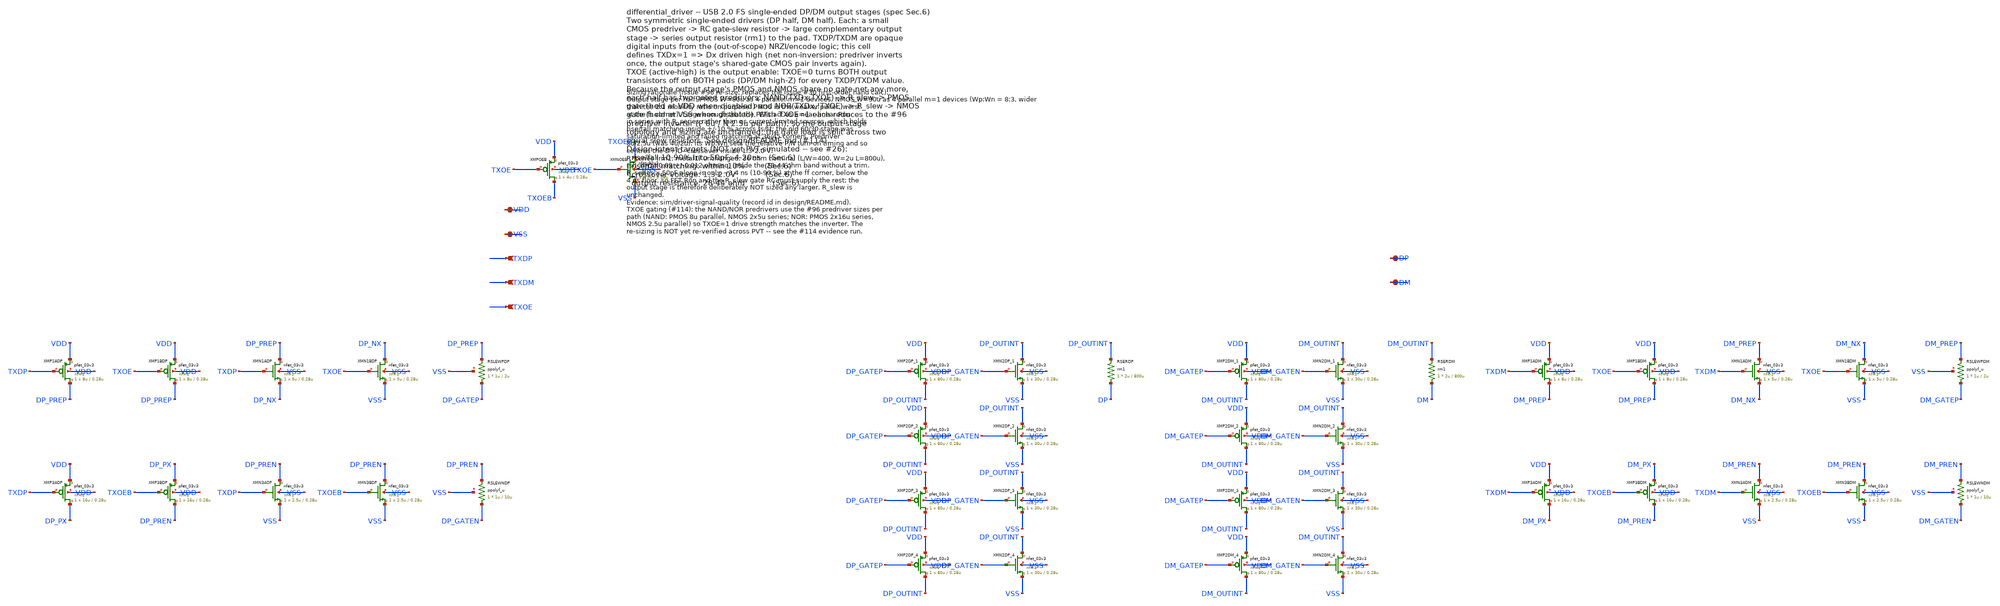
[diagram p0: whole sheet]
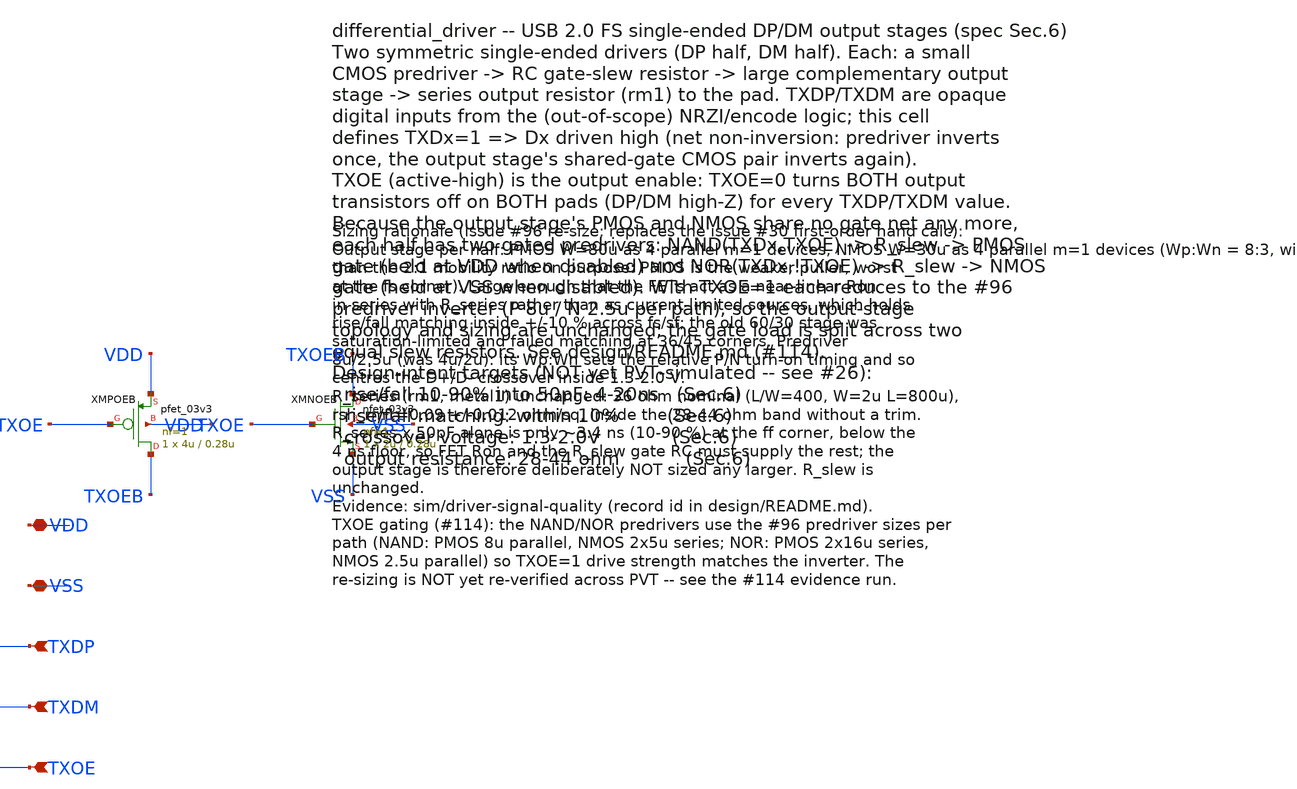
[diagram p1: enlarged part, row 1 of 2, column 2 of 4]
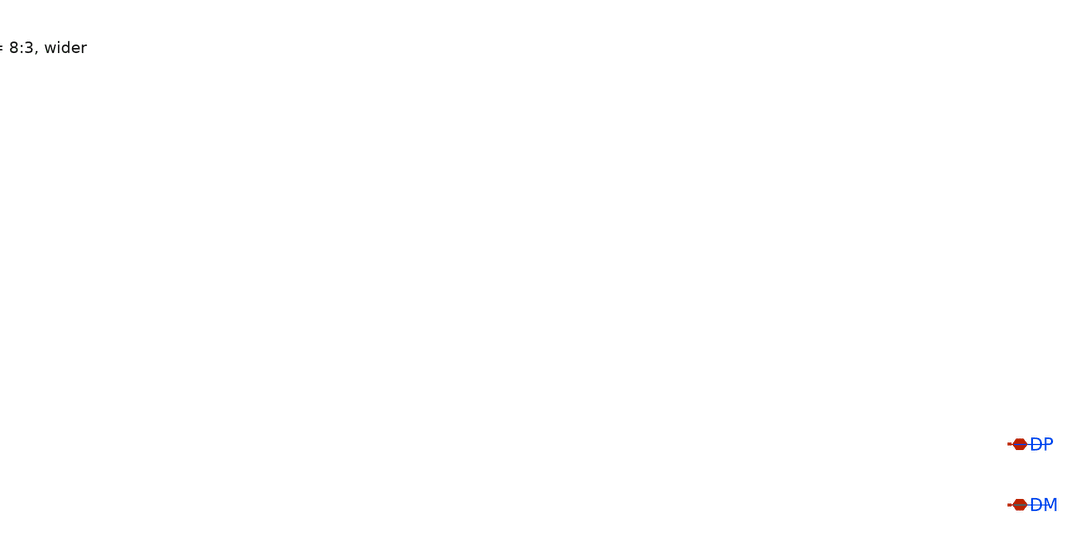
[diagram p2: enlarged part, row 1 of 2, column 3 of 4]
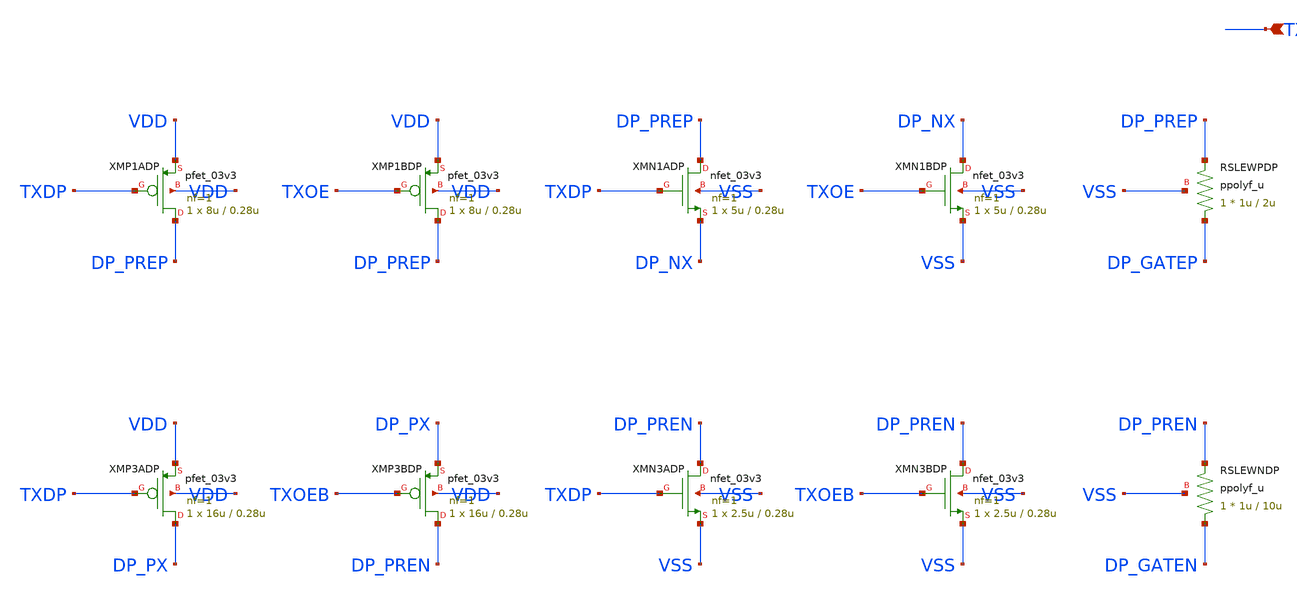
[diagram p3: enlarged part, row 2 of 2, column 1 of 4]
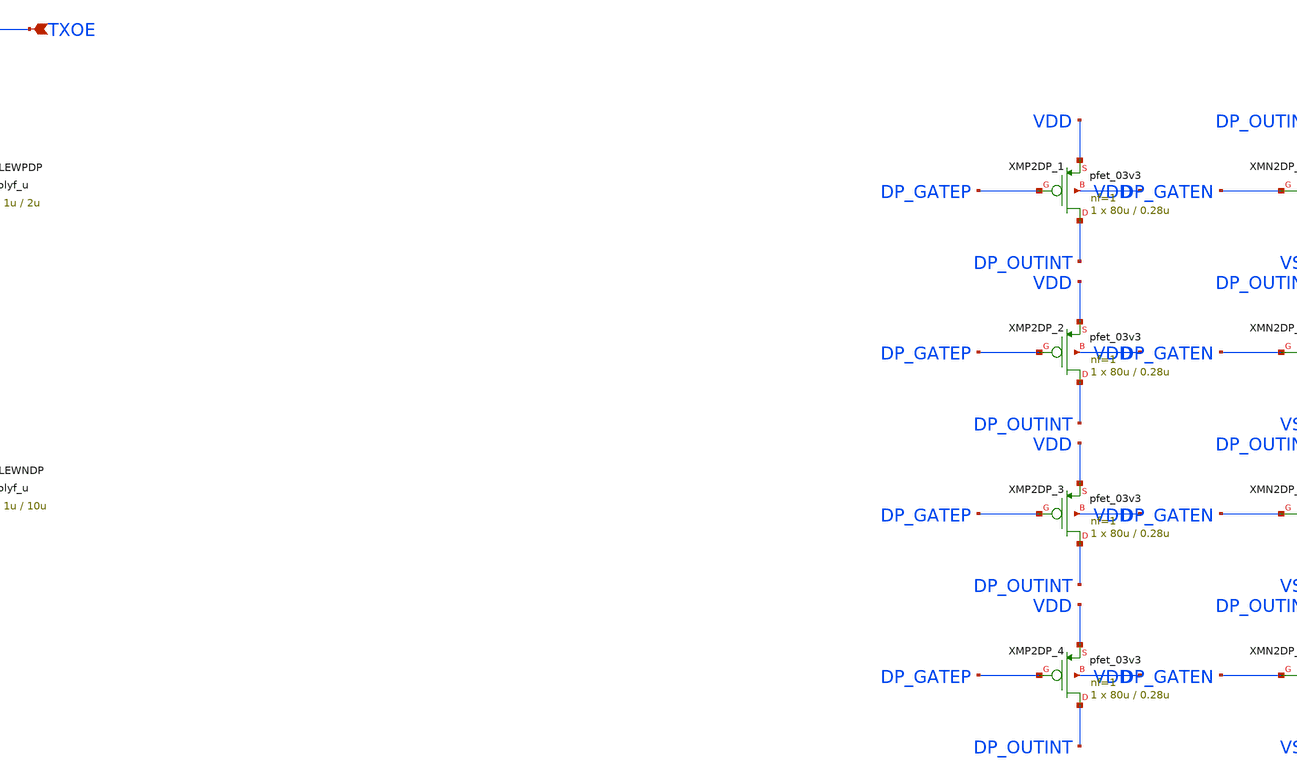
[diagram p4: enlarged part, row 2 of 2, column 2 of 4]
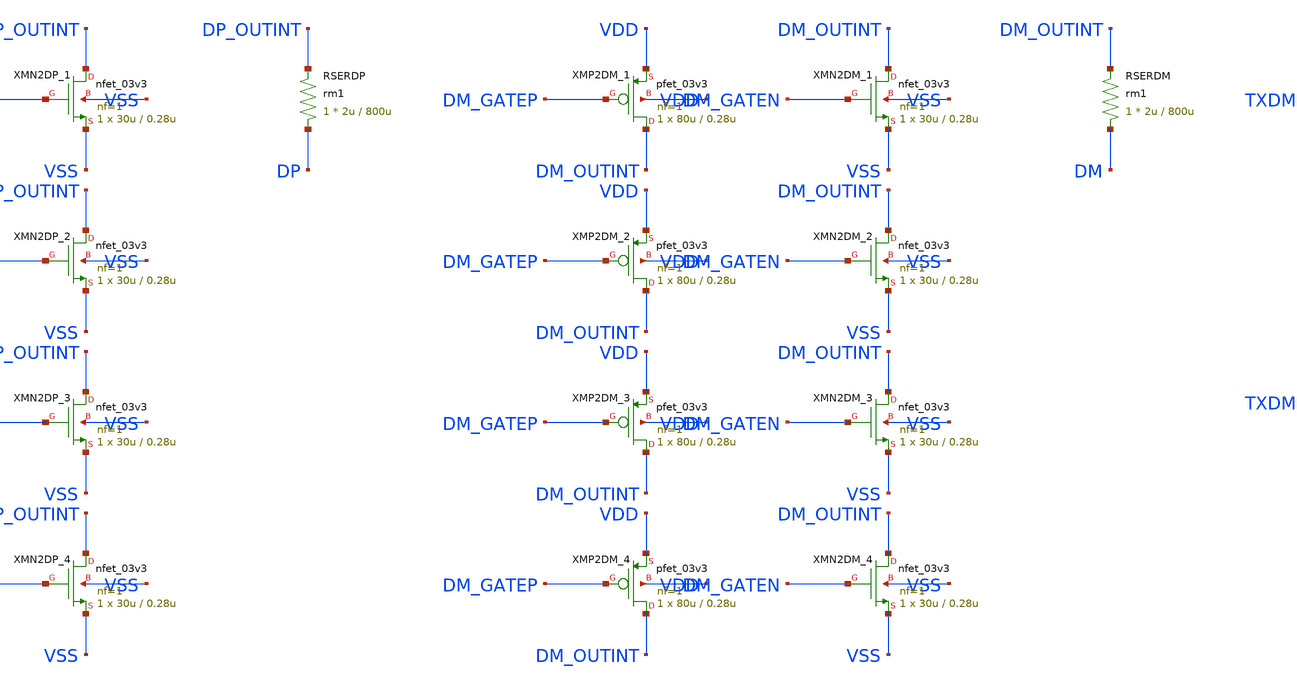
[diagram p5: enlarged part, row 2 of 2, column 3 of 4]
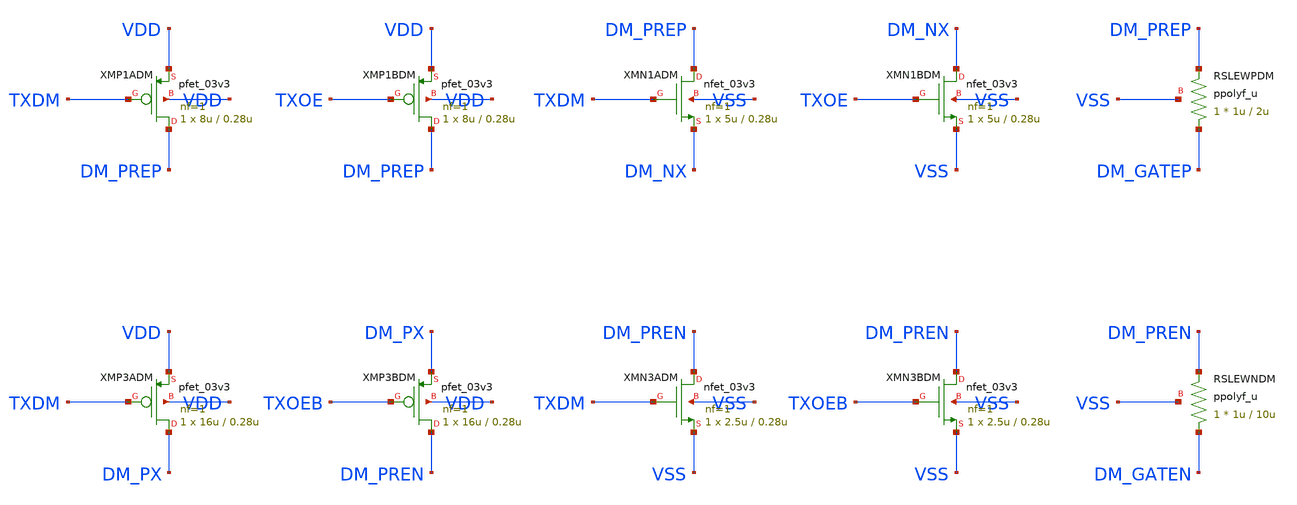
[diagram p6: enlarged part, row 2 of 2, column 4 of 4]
** sch_path: design/differential_driver.sch
**.subckt differential_driver VDD VSS TXDP TXDM TXOE DP DM
*.iopin VDD
*.iopin VSS
*.ipin TXDP
*.ipin TXDM
*.ipin TXOE
*.iopin DP
*.iopin DM
XMPOEB TXOEB TXOE VDD VDD pfet_03v3 L=0.28u W=4u nf=1 ad='int((nf+1)/2) * W/nf * 0.18u' as='int((nf+2)/2) * W/nf * 0.18u'
+ pd='2*int((nf+1)/2) * (W/nf + 0.18u)' ps='2*int((nf+2)/2) * (W/nf + 0.18u)' nrd='0.18u / W' nrs='0.18u / W'
+ sa=0 sb=0 sd=0 m=1
XMNOEB TXOEB TXOE VSS VSS nfet_03v3 L=0.28u W=2u nf=1 ad='int((nf+1)/2) * W/nf * 0.18u' as='int((nf+2)/2) * W/nf * 0.18u'
+ pd='2*int((nf+1)/2) * (W/nf + 0.18u)' ps='2*int((nf+2)/2) * (W/nf + 0.18u)' nrd='0.18u / W' nrs='0.18u / W'
+ sa=0 sb=0 sd=0 m=1
XMP1ADP DP_PREP TXDP VDD VDD pfet_03v3 L=0.28u W=8u nf=1 ad='int((nf+1)/2) * W/nf * 0.18u' as='int((nf+2)/2) * W/nf * 0.18u'
+ pd='2*int((nf+1)/2) * (W/nf + 0.18u)' ps='2*int((nf+2)/2) * (W/nf + 0.18u)' nrd='0.18u / W' nrs='0.18u / W'
+ sa=0 sb=0 sd=0 m=1
XMP1BDP DP_PREP TXOE VDD VDD pfet_03v3 L=0.28u W=8u nf=1 ad='int((nf+1)/2) * W/nf * 0.18u' as='int((nf+2)/2) * W/nf * 0.18u'
+ pd='2*int((nf+1)/2) * (W/nf + 0.18u)' ps='2*int((nf+2)/2) * (W/nf + 0.18u)' nrd='0.18u / W' nrs='0.18u / W'
+ sa=0 sb=0 sd=0 m=1
XMN1ADP DP_PREP TXDP DP_NX VSS nfet_03v3 L=0.28u W=5u nf=1 ad='int((nf+1)/2) * W/nf * 0.18u' as='int((nf+2)/2) * W/nf * 0.18u'
+ pd='2*int((nf+1)/2) * (W/nf + 0.18u)' ps='2*int((nf+2)/2) * (W/nf + 0.18u)' nrd='0.18u / W' nrs='0.18u / W'
+ sa=0 sb=0 sd=0 m=1
XMN1BDP DP_NX TXOE VSS VSS nfet_03v3 L=0.28u W=5u nf=1 ad='int((nf+1)/2) * W/nf * 0.18u' as='int((nf+2)/2) * W/nf * 0.18u'
+ pd='2*int((nf+1)/2) * (W/nf + 0.18u)' ps='2*int((nf+2)/2) * (W/nf + 0.18u)' nrd='0.18u / W' nrs='0.18u / W'
+ sa=0 sb=0 sd=0 m=1
XRSLEWPDP DP_GATEP DP_PREP VSS ppolyf_u r_width=1u r_length=2u m=1
XMP3ADP DP_PX TXDP VDD VDD pfet_03v3 L=0.28u W=16u nf=1 ad='int((nf+1)/2) * W/nf * 0.18u' as='int((nf+2)/2) * W/nf * 0.18u'
+ pd='2*int((nf+1)/2) * (W/nf + 0.18u)' ps='2*int((nf+2)/2) * (W/nf + 0.18u)' nrd='0.18u / W' nrs='0.18u / W'
+ sa=0 sb=0 sd=0 m=1
XMP3BDP DP_PREN TXOEB DP_PX VDD pfet_03v3 L=0.28u W=16u nf=1 ad='int((nf+1)/2) * W/nf * 0.18u' as='int((nf+2)/2) * W/nf * 0.18u'
+ pd='2*int((nf+1)/2) * (W/nf + 0.18u)' ps='2*int((nf+2)/2) * (W/nf + 0.18u)' nrd='0.18u / W' nrs='0.18u / W'
+ sa=0 sb=0 sd=0 m=1
XMN3ADP DP_PREN TXDP VSS VSS nfet_03v3 L=0.28u W=2.5u nf=1 ad='int((nf+1)/2) * W/nf * 0.18u' as='int((nf+2)/2) * W/nf * 0.18u'
+ pd='2*int((nf+1)/2) * (W/nf + 0.18u)' ps='2*int((nf+2)/2) * (W/nf + 0.18u)' nrd='0.18u / W' nrs='0.18u / W'
+ sa=0 sb=0 sd=0 m=1
XMN3BDP DP_PREN TXOEB VSS VSS nfet_03v3 L=0.28u W=2.5u nf=1 ad='int((nf+1)/2) * W/nf * 0.18u' as='int((nf+2)/2) * W/nf * 0.18u'
+ pd='2*int((nf+1)/2) * (W/nf + 0.18u)' ps='2*int((nf+2)/2) * (W/nf + 0.18u)' nrd='0.18u / W' nrs='0.18u / W'
+ sa=0 sb=0 sd=0 m=1
XRSLEWNDP DP_GATEN DP_PREN VSS ppolyf_u r_width=1u r_length=10u m=1
XMP2DP_1 DP_OUTINT DP_GATEP VDD VDD pfet_03v3 L=0.28u W=80u nf=1 ad='int((nf+1)/2) * W/nf * 0.18u' as='int((nf+2)/2) * W/nf * 0.18u'
+ pd='2*int((nf+1)/2) * (W/nf + 0.18u)' ps='2*int((nf+2)/2) * (W/nf + 0.18u)' nrd='0.18u / W' nrs='0.18u / W'
+ sa=0 sb=0 sd=0 m=1
XMP2DP_2 DP_OUTINT DP_GATEP VDD VDD pfet_03v3 L=0.28u W=80u nf=1 ad='int((nf+1)/2) * W/nf * 0.18u' as='int((nf+2)/2) * W/nf * 0.18u'
+ pd='2*int((nf+1)/2) * (W/nf + 0.18u)' ps='2*int((nf+2)/2) * (W/nf + 0.18u)' nrd='0.18u / W' nrs='0.18u / W'
+ sa=0 sb=0 sd=0 m=1
XMP2DP_3 DP_OUTINT DP_GATEP VDD VDD pfet_03v3 L=0.28u W=80u nf=1 ad='int((nf+1)/2) * W/nf * 0.18u' as='int((nf+2)/2) * W/nf * 0.18u'
+ pd='2*int((nf+1)/2) * (W/nf + 0.18u)' ps='2*int((nf+2)/2) * (W/nf + 0.18u)' nrd='0.18u / W' nrs='0.18u / W'
+ sa=0 sb=0 sd=0 m=1
XMP2DP_4 DP_OUTINT DP_GATEP VDD VDD pfet_03v3 L=0.28u W=80u nf=1 ad='int((nf+1)/2) * W/nf * 0.18u' as='int((nf+2)/2) * W/nf * 0.18u'
+ pd='2*int((nf+1)/2) * (W/nf + 0.18u)' ps='2*int((nf+2)/2) * (W/nf + 0.18u)' nrd='0.18u / W' nrs='0.18u / W'
+ sa=0 sb=0 sd=0 m=1
XMN2DP_1 DP_OUTINT DP_GATEN VSS VSS nfet_03v3 L=0.28u W=30u nf=1 ad='int((nf+1)/2) * W/nf * 0.18u' as='int((nf+2)/2) * W/nf * 0.18u'
+ pd='2*int((nf+1)/2) * (W/nf + 0.18u)' ps='2*int((nf+2)/2) * (W/nf + 0.18u)' nrd='0.18u / W' nrs='0.18u / W'
+ sa=0 sb=0 sd=0 m=1
XMN2DP_2 DP_OUTINT DP_GATEN VSS VSS nfet_03v3 L=0.28u W=30u nf=1 ad='int((nf+1)/2) * W/nf * 0.18u' as='int((nf+2)/2) * W/nf * 0.18u'
+ pd='2*int((nf+1)/2) * (W/nf + 0.18u)' ps='2*int((nf+2)/2) * (W/nf + 0.18u)' nrd='0.18u / W' nrs='0.18u / W'
+ sa=0 sb=0 sd=0 m=1
XMN2DP_3 DP_OUTINT DP_GATEN VSS VSS nfet_03v3 L=0.28u W=30u nf=1 ad='int((nf+1)/2) * W/nf * 0.18u' as='int((nf+2)/2) * W/nf * 0.18u'
+ pd='2*int((nf+1)/2) * (W/nf + 0.18u)' ps='2*int((nf+2)/2) * (W/nf + 0.18u)' nrd='0.18u / W' nrs='0.18u / W'
+ sa=0 sb=0 sd=0 m=1
XMN2DP_4 DP_OUTINT DP_GATEN VSS VSS nfet_03v3 L=0.28u W=30u nf=1 ad='int((nf+1)/2) * W/nf * 0.18u' as='int((nf+2)/2) * W/nf * 0.18u'
+ pd='2*int((nf+1)/2) * (W/nf + 0.18u)' ps='2*int((nf+2)/2) * (W/nf + 0.18u)' nrd='0.18u / W' nrs='0.18u / W'
+ sa=0 sb=0 sd=0 m=1
XRSERDP DP DP_OUTINT rm1 r_width=2u r_length=800u m=1
XMP1ADM DM_PREP TXDM VDD VDD pfet_03v3 L=0.28u W=8u nf=1 ad='int((nf+1)/2) * W/nf * 0.18u' as='int((nf+2)/2) * W/nf * 0.18u'
+ pd='2*int((nf+1)/2) * (W/nf + 0.18u)' ps='2*int((nf+2)/2) * (W/nf + 0.18u)' nrd='0.18u / W' nrs='0.18u / W'
+ sa=0 sb=0 sd=0 m=1
XMP1BDM DM_PREP TXOE VDD VDD pfet_03v3 L=0.28u W=8u nf=1 ad='int((nf+1)/2) * W/nf * 0.18u' as='int((nf+2)/2) * W/nf * 0.18u'
+ pd='2*int((nf+1)/2) * (W/nf + 0.18u)' ps='2*int((nf+2)/2) * (W/nf + 0.18u)' nrd='0.18u / W' nrs='0.18u / W'
+ sa=0 sb=0 sd=0 m=1
XMN1ADM DM_PREP TXDM DM_NX VSS nfet_03v3 L=0.28u W=5u nf=1 ad='int((nf+1)/2) * W/nf * 0.18u' as='int((nf+2)/2) * W/nf * 0.18u'
+ pd='2*int((nf+1)/2) * (W/nf + 0.18u)' ps='2*int((nf+2)/2) * (W/nf + 0.18u)' nrd='0.18u / W' nrs='0.18u / W'
+ sa=0 sb=0 sd=0 m=1
XMN1BDM DM_NX TXOE VSS VSS nfet_03v3 L=0.28u W=5u nf=1 ad='int((nf+1)/2) * W/nf * 0.18u' as='int((nf+2)/2) * W/nf * 0.18u'
+ pd='2*int((nf+1)/2) * (W/nf + 0.18u)' ps='2*int((nf+2)/2) * (W/nf + 0.18u)' nrd='0.18u / W' nrs='0.18u / W'
+ sa=0 sb=0 sd=0 m=1
XRSLEWPDM DM_GATEP DM_PREP VSS ppolyf_u r_width=1u r_length=2u m=1
XMP3ADM DM_PX TXDM VDD VDD pfet_03v3 L=0.28u W=16u nf=1 ad='int((nf+1)/2) * W/nf * 0.18u' as='int((nf+2)/2) * W/nf * 0.18u'
+ pd='2*int((nf+1)/2) * (W/nf + 0.18u)' ps='2*int((nf+2)/2) * (W/nf + 0.18u)' nrd='0.18u / W' nrs='0.18u / W'
+ sa=0 sb=0 sd=0 m=1
XMP3BDM DM_PREN TXOEB DM_PX VDD pfet_03v3 L=0.28u W=16u nf=1 ad='int((nf+1)/2) * W/nf * 0.18u' as='int((nf+2)/2) * W/nf * 0.18u'
+ pd='2*int((nf+1)/2) * (W/nf + 0.18u)' ps='2*int((nf+2)/2) * (W/nf + 0.18u)' nrd='0.18u / W' nrs='0.18u / W'
+ sa=0 sb=0 sd=0 m=1
XMN3ADM DM_PREN TXDM VSS VSS nfet_03v3 L=0.28u W=2.5u nf=1 ad='int((nf+1)/2) * W/nf * 0.18u' as='int((nf+2)/2) * W/nf * 0.18u'
+ pd='2*int((nf+1)/2) * (W/nf + 0.18u)' ps='2*int((nf+2)/2) * (W/nf + 0.18u)' nrd='0.18u / W' nrs='0.18u / W'
+ sa=0 sb=0 sd=0 m=1
XMN3BDM DM_PREN TXOEB VSS VSS nfet_03v3 L=0.28u W=2.5u nf=1 ad='int((nf+1)/2) * W/nf * 0.18u' as='int((nf+2)/2) * W/nf * 0.18u'
+ pd='2*int((nf+1)/2) * (W/nf + 0.18u)' ps='2*int((nf+2)/2) * (W/nf + 0.18u)' nrd='0.18u / W' nrs='0.18u / W'
+ sa=0 sb=0 sd=0 m=1
XRSLEWNDM DM_GATEN DM_PREN VSS ppolyf_u r_width=1u r_length=10u m=1
XMP2DM_1 DM_OUTINT DM_GATEP VDD VDD pfet_03v3 L=0.28u W=80u nf=1 ad='int((nf+1)/2) * W/nf * 0.18u' as='int((nf+2)/2) * W/nf * 0.18u'
+ pd='2*int((nf+1)/2) * (W/nf + 0.18u)' ps='2*int((nf+2)/2) * (W/nf + 0.18u)' nrd='0.18u / W' nrs='0.18u / W'
+ sa=0 sb=0 sd=0 m=1
XMP2DM_2 DM_OUTINT DM_GATEP VDD VDD pfet_03v3 L=0.28u W=80u nf=1 ad='int((nf+1)/2) * W/nf * 0.18u' as='int((nf+2)/2) * W/nf * 0.18u'
+ pd='2*int((nf+1)/2) * (W/nf + 0.18u)' ps='2*int((nf+2)/2) * (W/nf + 0.18u)' nrd='0.18u / W' nrs='0.18u / W'
+ sa=0 sb=0 sd=0 m=1
XMP2DM_3 DM_OUTINT DM_GATEP VDD VDD pfet_03v3 L=0.28u W=80u nf=1 ad='int((nf+1)/2) * W/nf * 0.18u' as='int((nf+2)/2) * W/nf * 0.18u'
+ pd='2*int((nf+1)/2) * (W/nf + 0.18u)' ps='2*int((nf+2)/2) * (W/nf + 0.18u)' nrd='0.18u / W' nrs='0.18u / W'
+ sa=0 sb=0 sd=0 m=1
XMP2DM_4 DM_OUTINT DM_GATEP VDD VDD pfet_03v3 L=0.28u W=80u nf=1 ad='int((nf+1)/2) * W/nf * 0.18u' as='int((nf+2)/2) * W/nf * 0.18u'
+ pd='2*int((nf+1)/2) * (W/nf + 0.18u)' ps='2*int((nf+2)/2) * (W/nf + 0.18u)' nrd='0.18u / W' nrs='0.18u / W'
+ sa=0 sb=0 sd=0 m=1
XMN2DM_1 DM_OUTINT DM_GATEN VSS VSS nfet_03v3 L=0.28u W=30u nf=1 ad='int((nf+1)/2) * W/nf * 0.18u' as='int((nf+2)/2) * W/nf * 0.18u'
+ pd='2*int((nf+1)/2) * (W/nf + 0.18u)' ps='2*int((nf+2)/2) * (W/nf + 0.18u)' nrd='0.18u / W' nrs='0.18u / W'
+ sa=0 sb=0 sd=0 m=1
XMN2DM_2 DM_OUTINT DM_GATEN VSS VSS nfet_03v3 L=0.28u W=30u nf=1 ad='int((nf+1)/2) * W/nf * 0.18u' as='int((nf+2)/2) * W/nf * 0.18u'
+ pd='2*int((nf+1)/2) * (W/nf + 0.18u)' ps='2*int((nf+2)/2) * (W/nf + 0.18u)' nrd='0.18u / W' nrs='0.18u / W'
+ sa=0 sb=0 sd=0 m=1
XMN2DM_3 DM_OUTINT DM_GATEN VSS VSS nfet_03v3 L=0.28u W=30u nf=1 ad='int((nf+1)/2) * W/nf * 0.18u' as='int((nf+2)/2) * W/nf * 0.18u'
+ pd='2*int((nf+1)/2) * (W/nf + 0.18u)' ps='2*int((nf+2)/2) * (W/nf + 0.18u)' nrd='0.18u / W' nrs='0.18u / W'
+ sa=0 sb=0 sd=0 m=1
XMN2DM_4 DM_OUTINT DM_GATEN VSS VSS nfet_03v3 L=0.28u W=30u nf=1 ad='int((nf+1)/2) * W/nf * 0.18u' as='int((nf+2)/2) * W/nf * 0.18u'
+ pd='2*int((nf+1)/2) * (W/nf + 0.18u)' ps='2*int((nf+2)/2) * (W/nf + 0.18u)' nrd='0.18u / W' nrs='0.18u / W'
+ sa=0 sb=0 sd=0 m=1
XRSERDM DM DM_OUTINT rm1 r_width=2u r_length=800u m=1
**.ends
.end
